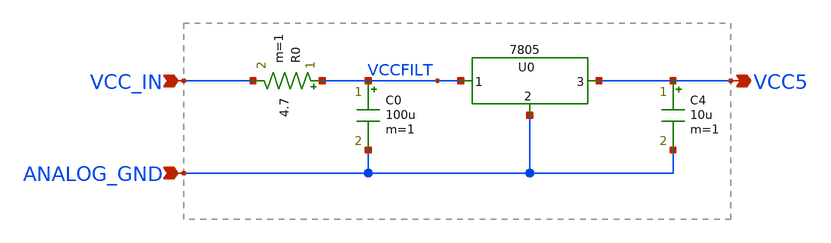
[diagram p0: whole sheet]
** sch_path: xschem_libs_newsym/pcb/reg/schematic/reg.sch
* Copyright (C) 1998-2024 Stefan Frederik Schippers
* This program is free software; you can redistribute it and/or modify
* it under the terms of the GNU General Public License as published by
* the Free Software Foundation; either version 2 of the License, or
* (at your option) any later version.
* This program is distributed in the hope that it will be useful,
* but WITHOUT ANY WARRANTY; without even the implied warranty of
* MERCHANTABILITY or FITNESS FOR A PARTICULAR PURPOSE.  See the
* GNU General Public License for more details.
* You should have received a copy of the GNU General Public License
* along with this program; if not, write to the Free Software
**.subckt reg VCC5 VCC_IN ANALOG_GND
*.opin VCC5
*.ipin VCC_IN
*.ipin ANALOG_GND
C0 VCCFILT ANALOG_GND 100u m=1
XU0 VCCFILT ANALOG_GND VCC5 7805
C4 VCC5 ANALOG_GND 10u m=1
R0 VCCFILT VCC_IN 4.7 m=1
**.ends
.end
